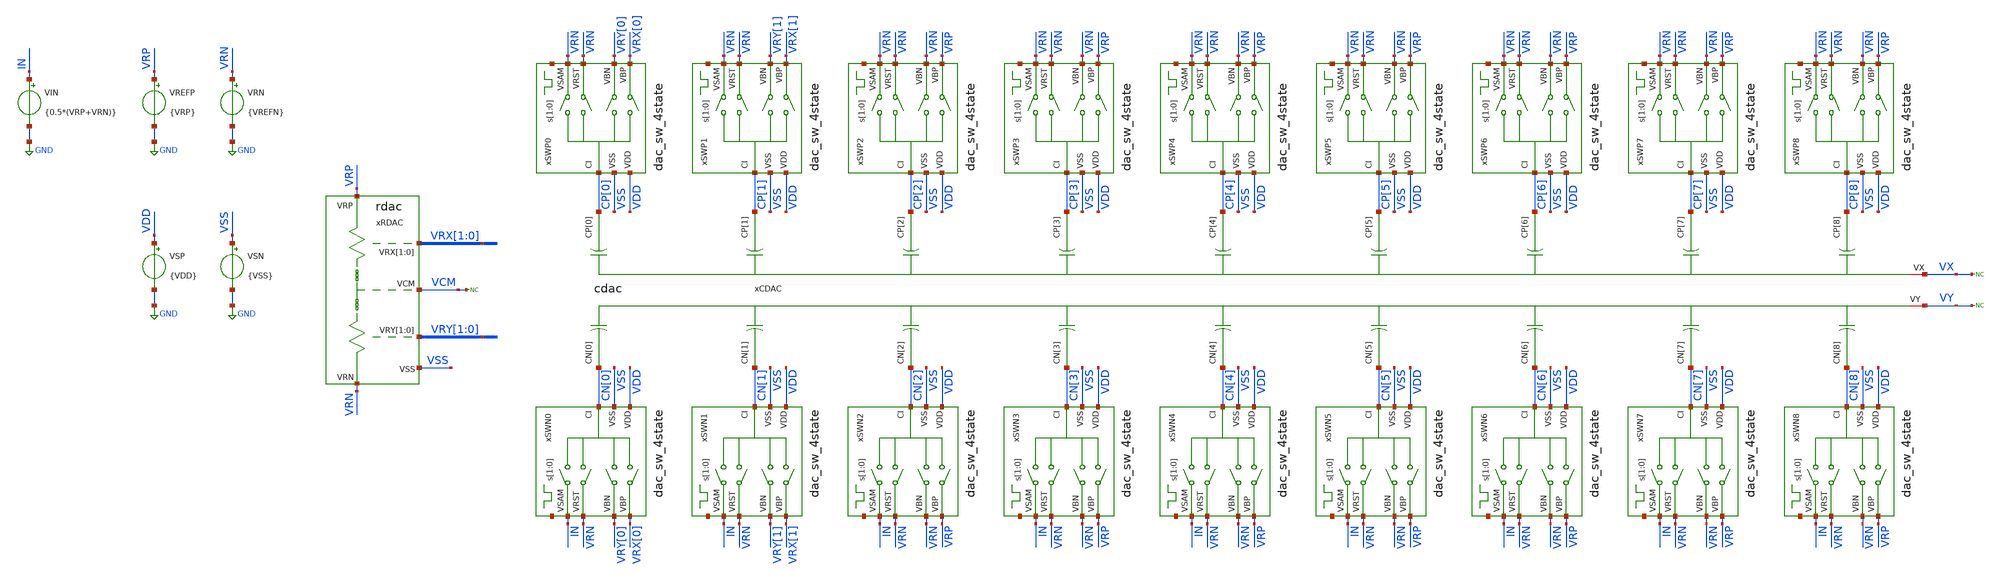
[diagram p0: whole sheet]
** sch_path: designs/sar_adc/dac/cdac/xschem/hybridRCDAC_TB.sch
**.subckt hybridRCDAC_TB
xCDAC CP[8] CP[3] CP[5] CP[1] CP[0] CP[4] CP[6] CP[7] CP[2] CN[2] CN[1] CN[3] CN[8] CN[7] CN[6]
+ CN[5] CN[4] CN[0] VX VY cdac
xRDAC VCM VRX[1] VRX[0] VRY[1] VRY[0] VRP VRN VSS rdac
* noconn VY
xSWP0 VDD net1[1] net1[0] VSS CP[0] VRN VRX[0] VRY[0] VRN dac_sw_4state
xSWP1 VDD net2[1] net2[0] VSS CP[1] VRN VRX[1] VRY[1] VRN dac_sw_4state
xSWP2 VDD net3[1] net3[0] VSS CP[2] VRN VRP VRN VRN dac_sw_4state
xSWP3 VDD net4[1] net4[0] VSS CP[3] VRN VRP VRN VRN dac_sw_4state
xSWP4 VDD net5[1] net5[0] VSS CP[4] VRN VRP VRN VRN dac_sw_4state
xSWP5 VDD net6[1] net6[0] VSS CP[5] VRN VRP VRN VRN dac_sw_4state
xSWP6 VDD net7[1] net7[0] VSS CP[6] VRN VRP VRN VRN dac_sw_4state
xSWP7 VDD net8[1] net8[0] VSS CP[7] VRN VRP VRN VRN dac_sw_4state
xSWP8 VDD net9[1] net9[0] VSS CP[8] VRN VRP VRN VRN dac_sw_4state
* noconn VX
xSWN0 VDD net10[1] net10[0] VSS CN[0] IN VRX[0] VRY[0] VRN dac_sw_4state
xSWN1 VDD net11[1] net11[0] VSS CN[1] IN VRX[1] VRY[1] VRN dac_sw_4state
xSWN2 VDD net12[1] net12[0] VSS CN[2] IN VRP VRN VRN dac_sw_4state
xSWN3 VDD net13[1] net13[0] VSS CN[3] IN VRP VRN VRN dac_sw_4state
xSWN4 VDD net14[1] net14[0] VSS CN[4] IN VRP VRN VRN dac_sw_4state
xSWN5 VDD net15[1] net15[0] VSS CN[5] IN VRP VRN VRN dac_sw_4state
xSWN6 VDD net16[1] net16[0] VSS CN[6] IN VRP VRN VRN dac_sw_4state
xSWN7 VDD net17[1] net17[0] VSS CN[7] IN VRP VRN VRN dac_sw_4state
xSWN8 VDD net18[1] net18[0] VSS CN[8] IN VRP VRN VRN dac_sw_4state
VSP VDD GND {VDD}
VSN VSS GND {VSS}
VREFP VRP GND {VRP}
VRN VRN GND {VREFN}
* noconn VCM
VIN IN GND {0.5*(VRP+VRN)}
**.ends
.GLOBAL GND
.end
